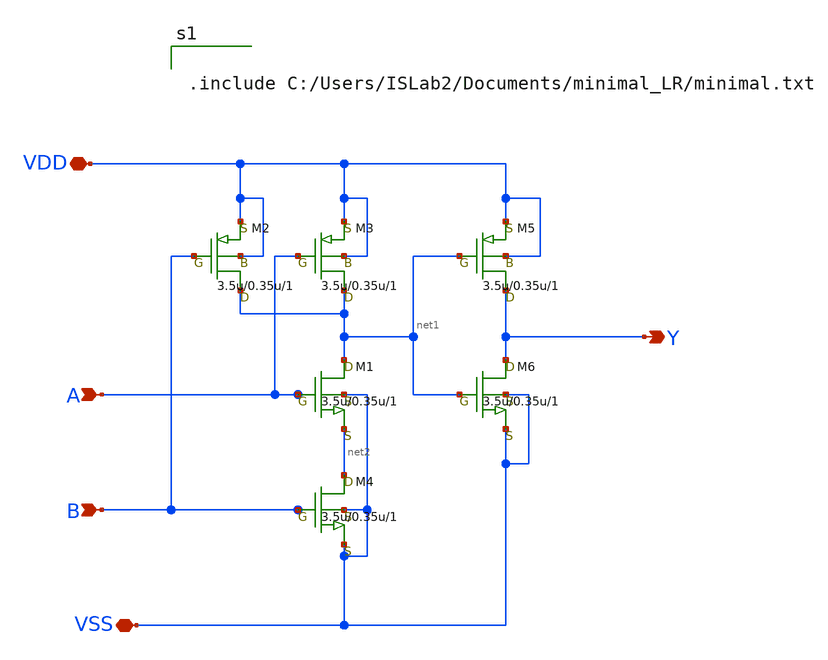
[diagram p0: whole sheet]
** sch_path: AND.sch
**.subckt AND VDD A B VSS Y
*.iopin VDD
*.ipin A
*.ipin B
*.iopin VSS
*.opin Y
M1 net1 A net2 VSS nch w=3.5u l=0.35u as=0 ps=0 ad=0 pd=0 m=1
M2 net1 B VDD VDD pch w=3.5u l=0.35u as=0 ps=0 ad=0 pd=0 m=1
M3 net1 A VDD VDD pch w=3.5u l=0.35u as=0 ps=0 ad=0 pd=0 m=1
M4 net2 B VSS VSS nch w=3.5u l=0.35u as=0 ps=0 ad=0 pd=0 m=1
M5 Y net1 VDD VDD pch w=3.5u l=0.35u as=0 ps=0 ad=0 pd=0 m=1
M6 Y net1 VSS VSS nch w=3.5u l=0.35u as=0 ps=0 ad=0 pd=0 m=1
**** begin user architecture code


.include C:/Users/ISLab2/Documents/minimal_LR/minimal.txt

**** end user architecture code
**.ends
.end
